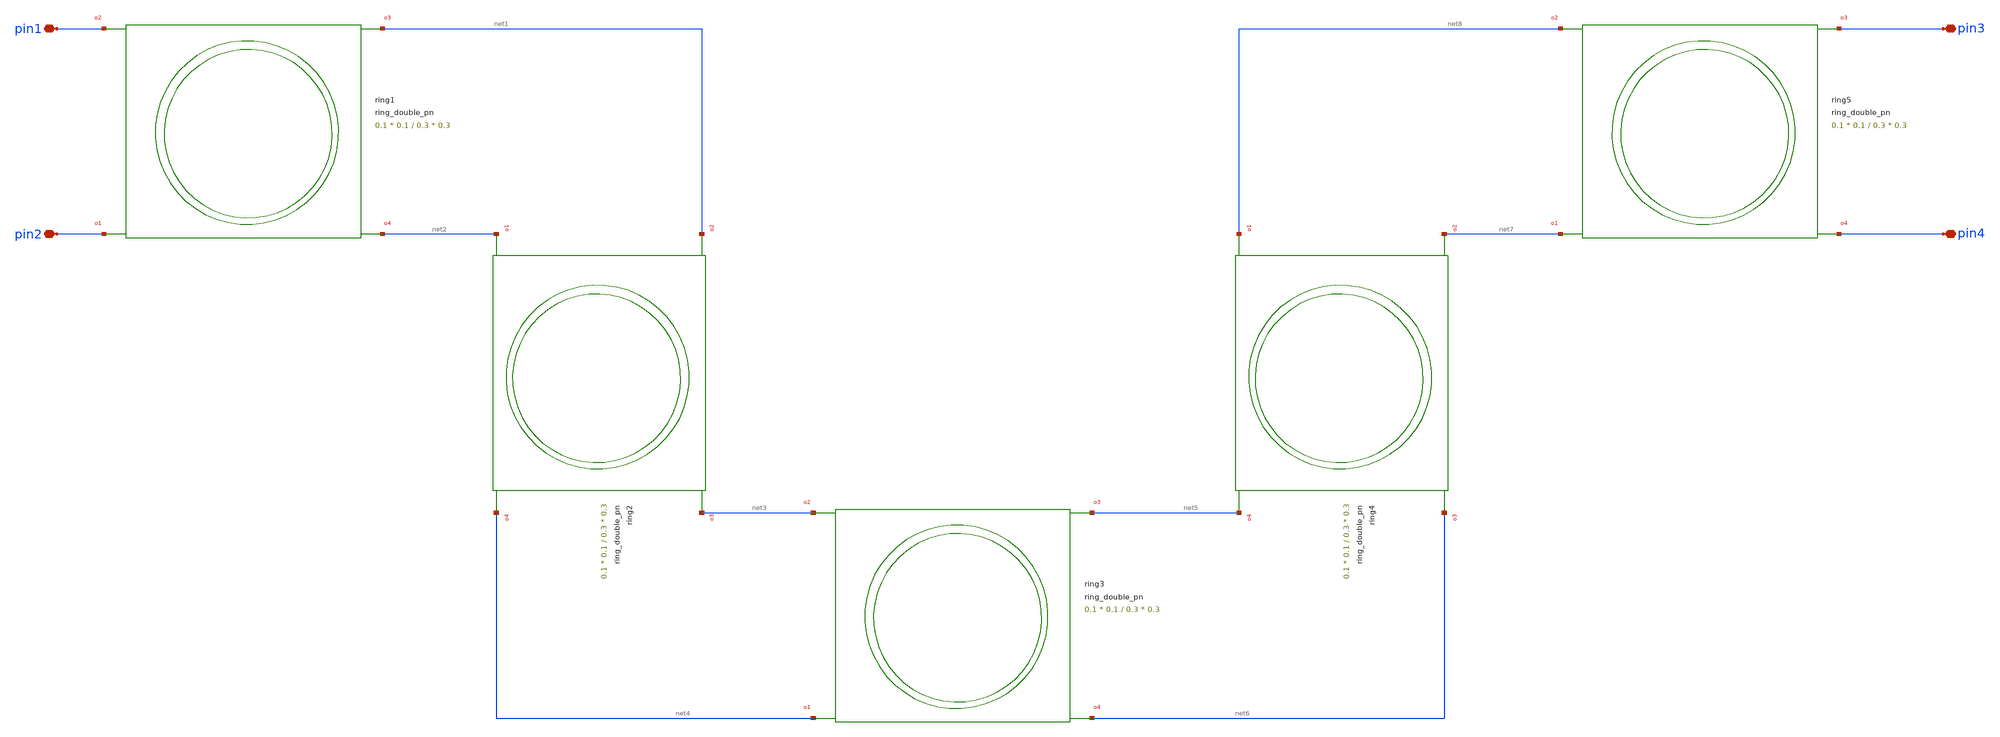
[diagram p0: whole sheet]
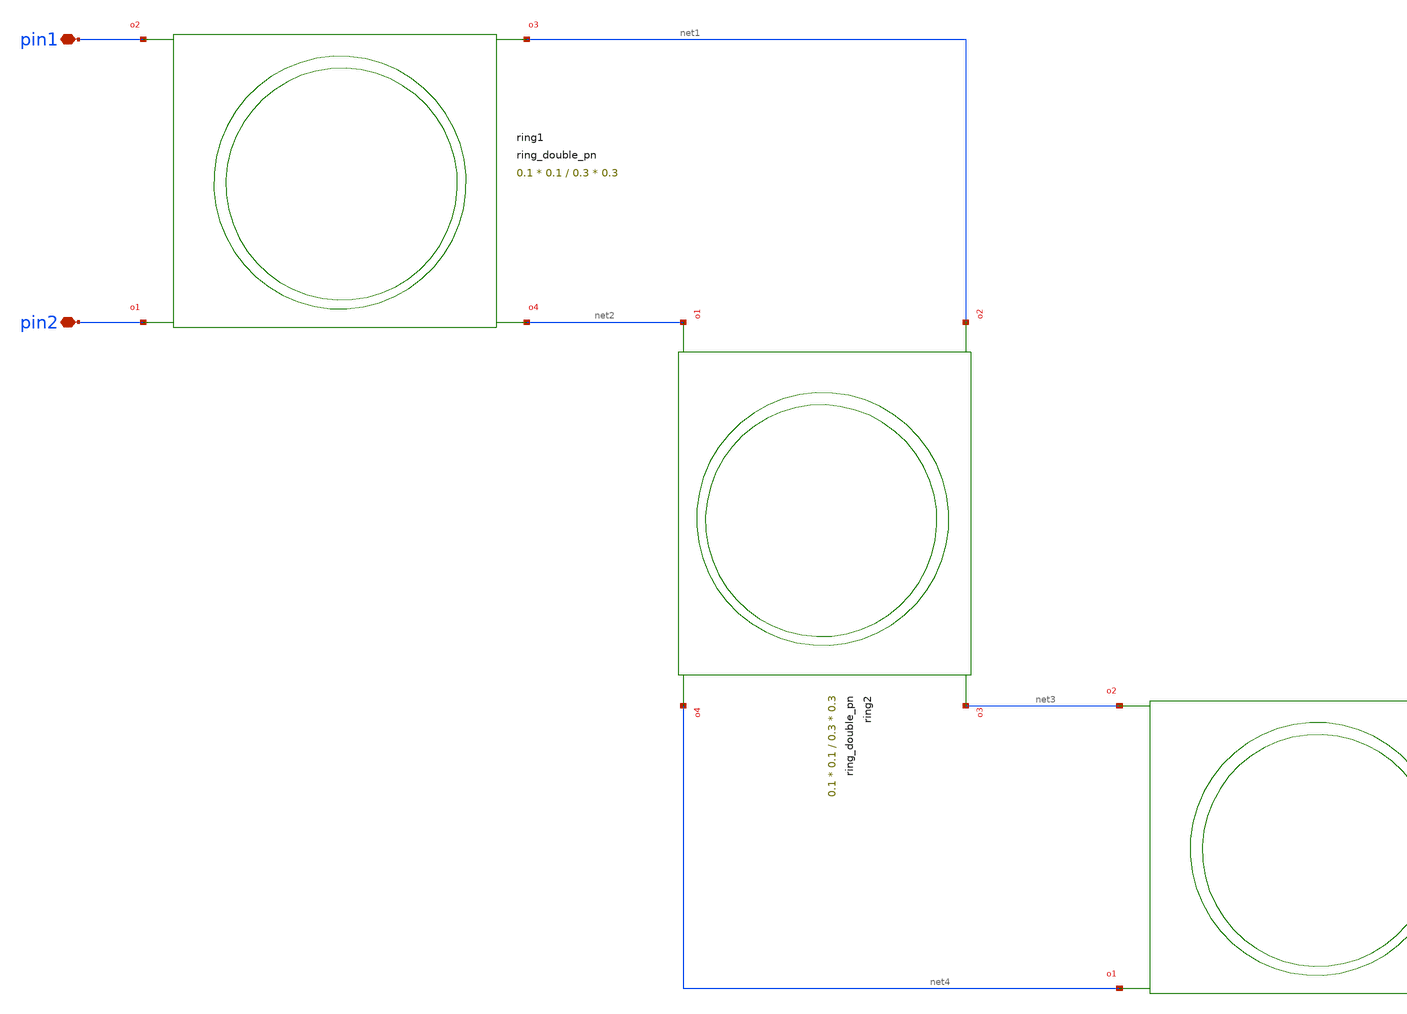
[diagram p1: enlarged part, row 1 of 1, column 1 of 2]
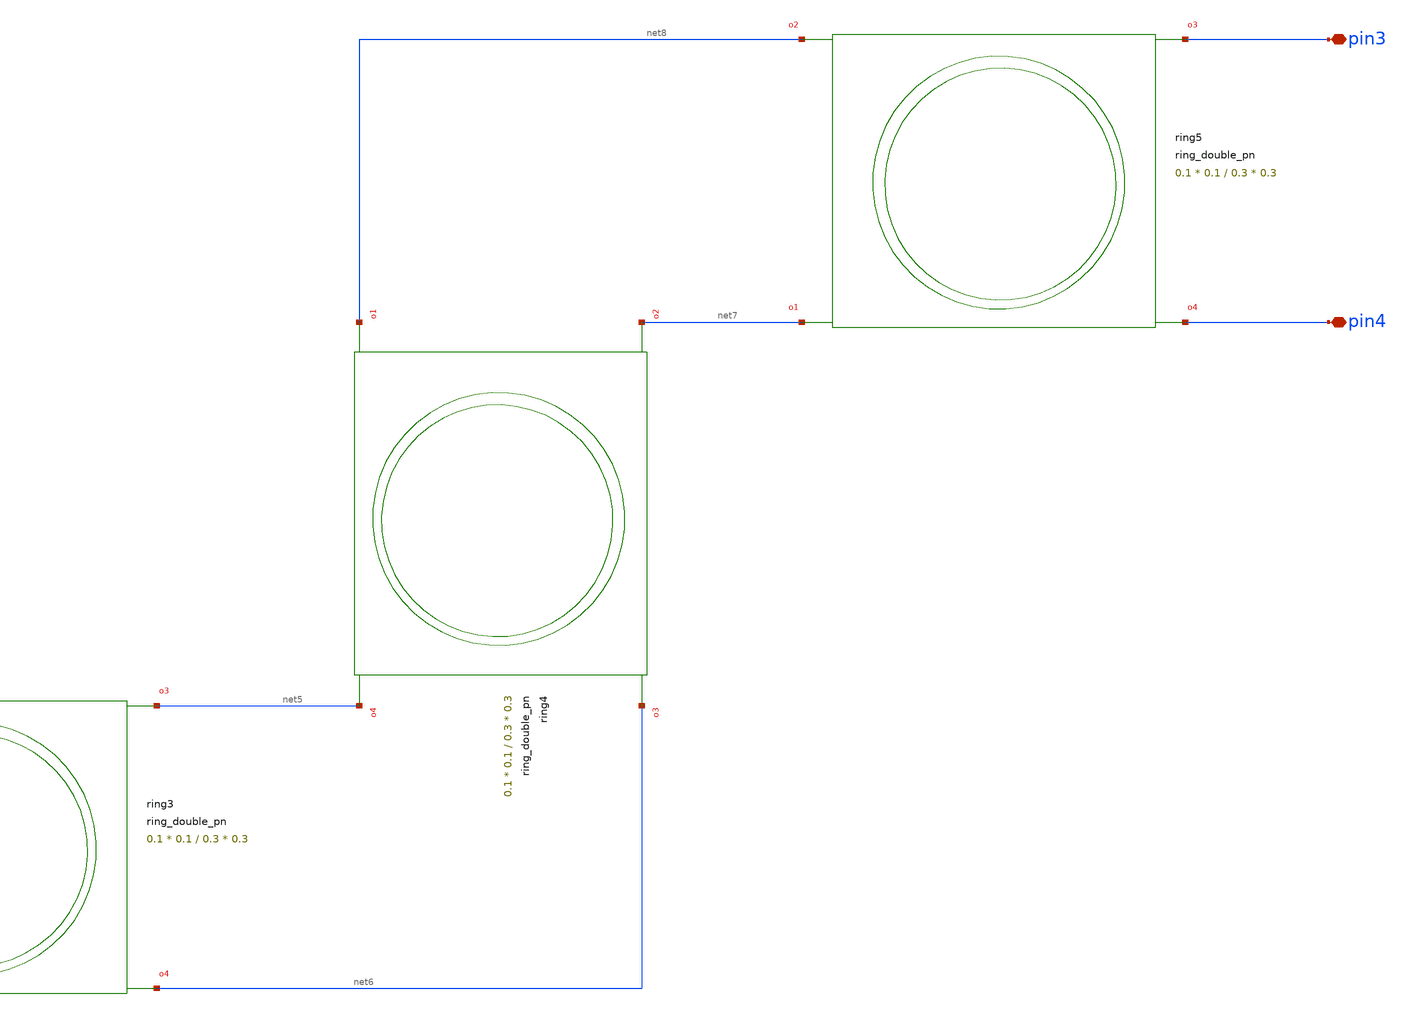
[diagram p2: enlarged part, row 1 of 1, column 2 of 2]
** sch_path: cells/xschem/tests/test_ring_double_pn.sch
* SPDX-FileCopyrightText: 2023 Mabrains Company
* Licensed under the GNU GENERAL PUBLIC License, Version 3.0 (the "License");
* you may not use this file except in compliance with the License.
* GNU GENERAL PUBLIC LICENSE
* Version 3, 29 June 2007
* This program is free software: you can redistribute it and/or modify
* it under the terms of the GNU General Public License as published
* by the Free Software Foundation, either 3 of the License, or
* (at your option) any later version.
* This program is distributed in the hope that it will be useful,
* but WITHOUT ANY WARRANTY; without even the implied warranty of
* MERCHANTABILITY or FITNESS FOR A PARTICULAR PURPOSE.  See the
* GNU General Public License for more details.
* You should have received a copy of the GNU General Public License
* along with this program.  If not, see <https://www.gnu.org/licenses/>.
* SPDX-License-Identifier: GPL-3.0
**.subckt test_ring_double_pn pin1 pin2 pin3 pin4
*.iopin pin1
*.iopin pin2
*.iopin pin3
*.iopin pin4
Pring1 pin2 pin1 net1 net2 ring_double_pn add_gap=0.3 drop_gap=0.3 radius=5.0 doping_angle=85
+ length_x=0.1 length_y=0.1
Pring2 net2 net1 net3 net4 ring_double_pn add_gap=0.3 drop_gap=0.3 radius=5.0 doping_angle=85
+ length_x=0.1 length_y=0.1
Pring3 net4 net3 net5 net6 ring_double_pn add_gap=0.3 drop_gap=0.3 radius=5.0 doping_angle=85
+ length_x=0.1 length_y=0.1
Pring4 net8 net7 net6 net5 ring_double_pn add_gap=0.3 drop_gap=0.3 radius=5.0 doping_angle=85
+ length_x=0.1 length_y=0.1
Pring5 net7 net8 pin3 pin4 ring_double_pn add_gap=0.3 drop_gap=0.3 radius=5.0 doping_angle=85
+ length_x=0.1 length_y=0.1
**.ends
.end
